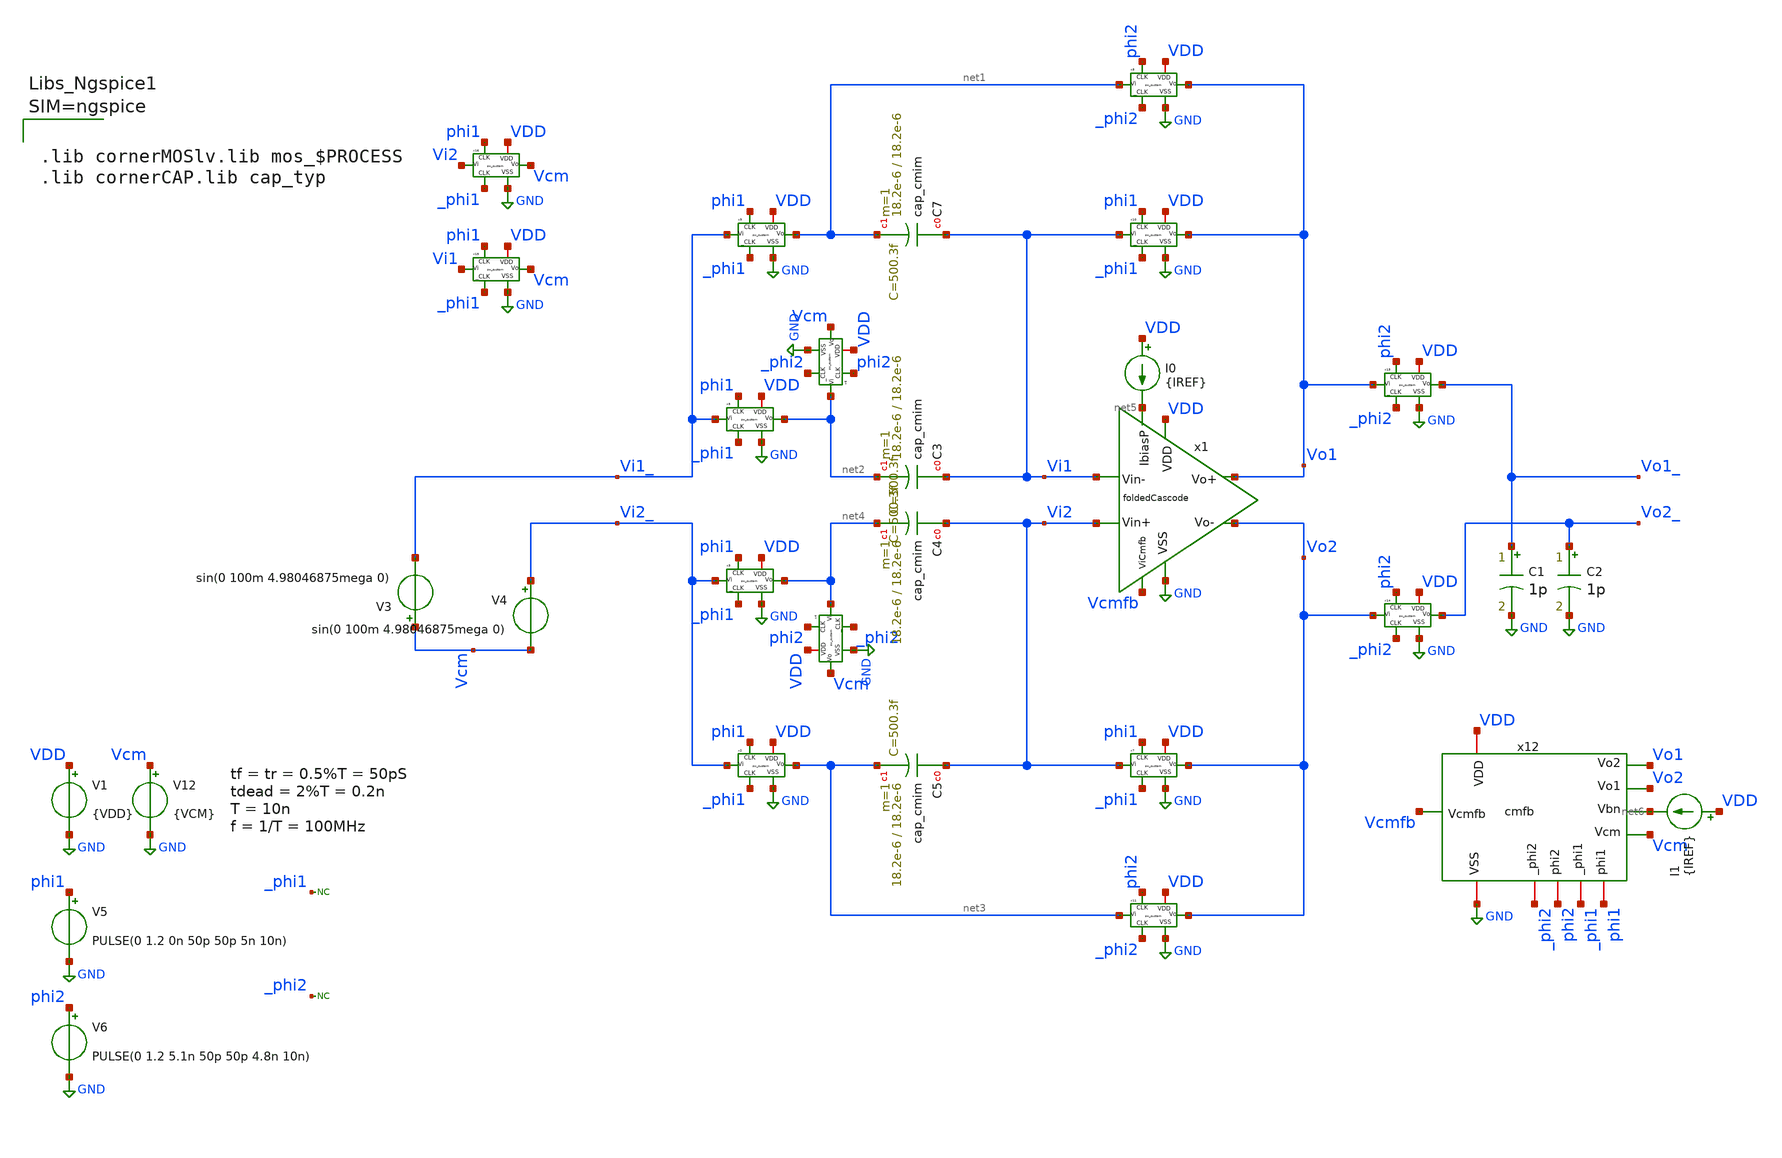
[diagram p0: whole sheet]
** sch_path: sch/AutoTestbench/tb/closeLoop.sch
**.subckt closeLoop
x1 VDD GND Vcmfb net5 Vo1 Vo2 Vi1 Vi2 foldedCascode
V1 VDD GND {VDD}
I0 VDD net5 {IREF}
V5 phi1 GND PULSE(0 1.2 0n 50p 50p 5n 10n)
V6 phi2 GND PULSE(0 1.2 5.1n 50p 50p 4.8n 10n)
x2 phi1 GND net3 Vi2_ VDD _phi1 sw_custom
x3 phi1 GND net4 Vi2_ VDD _phi1 sw_custom
x6 phi2 GND Vcm net2 VDD _phi2 sw_custom
x7 phi1 GND Vo2 Vi2 VDD _phi1 sw_custom
x8 phi2 GND Vo1 net1 VDD _phi2 sw_custom
x10 phi1 GND Vo1 Vi1 VDD _phi1 sw_custom
x9 phi1 GND net1 Vi1_ VDD _phi1 sw_custom
x11 phi2 GND Vo2 net3 VDD _phi2 sw_custom
x12 VDD GND phi1 _phi1 phi2 _phi2 Vcm net6 Vcmfb Vo2 Vo1 cmfb
x5 phi1 GND net2 Vi1_ VDD _phi1 sw_custom
x13 phi2 GND Vo1_ Vo1 VDD _phi2 sw_custom
x14 phi2 GND Vo2_ Vo2 VDD _phi2 sw_custom
V12 Vcm GND {VCM}
x15 phi1 GND Vcm Vi1 VDD _phi1 sw_custom
x16 phi1 GND Vcm Vi2 VDD _phi1 sw_custom
V3 Vcm Vi1_ sin(0 100m 4.98046875mega 0)
V4 Vi2_ Vcm sin(0 100m 4.98046875mega 0)
C1 Vo1_ GND 1p m=1
C2 Vo2_ GND 1p m=1
x4 phi2 GND Vcm net4 VDD _phi2 sw_custom
* noconn _phi1
* noconn _phi2
XC7 Vi1 net1 cap_cmim w=18.2e-6 l=18.2e-6 m=1 mm_ok=1
XC3 Vi1 net2 cap_cmim w=18.2e-6 l=18.2e-6 m=1 mm_ok=1
XC4 Vi2 net4 cap_cmim w=18.2e-6 l=18.2e-6 m=1 mm_ok=1
XC5 Vi2 net3 cap_cmim w=18.2e-6 l=18.2e-6 m=1 mm_ok=1
I1 VDD net6 {IREF}
**** begin user architecture code



.lib cornerMOSlv.lib mos_$PROCESS
.lib cornerCAP.lib cap_typ





.temp $TEMP
.model SW1 SW(Ron=50 Roff=10G Vt=0.4 Vh=0.1)
.nodeset v(Vo1)=0.6 v(Vo2)=0.6 v(Vi1)=0.6 v(Vi2)=0.6
.param VDD=$VDD
.param IREF=$IREF
.param VCM=$VCM
.control
op
tran 100p 12u
let vcm = (v(Vo1) + v(Vo2)) / 2
meas tran vcm_avg AVG vcm FROM=1u TO=3u
let Vinn = v(Vi1_)-v(Vi2_)
let Voutt = v(Vo1_)-v(Vo2_)
meas tran vin_pp  PP Vinn from=1u to=3u
meas tran vout_pp PP Voutt from=1u to=3u

let gain = vout_pp/vin_pp
print gain

let vcm_ = vcm_avg

echo Gain $&gain > results.txt
echo Vcm $&vcm_ >> results.txt

plot v(Vo1_)-v(Vo2_) v(phi2)

plot gain

write closeLoop.raw
*plot v(Vo1_) v(phi1)
plot v(Vo1_) v(Vi1_)
plot V(Vcmfb)
*plot v(Vo1)
plot v(vo1)
plot v(Vo1_)-v(Vo2_)
plot v(Vo1_) v(phi1) v(phi2)
*plot phi1 phi2


wrdata output.txt v(phi1) v(phi2) v(Vi1_) v(Vi2_) v(Vo1_) v(Vo2_)

.endc


**** end user architecture code
**.ends

* expanding   symbol:  foldedCascode.sym # of pins=8
** sym_path: sch/blocks/foldedCascode.sym
** sch_path: sch/blocks/foldedCascode.sch
.subckt foldedCascode VDD VSS ViCmfb IbiasP Vo+ Vo- Vin- Vin+
*.iopin VSS
*.iopin VDD
*.ipin ViCmfb
*.iopin IbiasP
*.ipin Vin+
*.ipin Vin-
*.iopin Vo+
*.iopin Vo-
x1 VDD Vb1_1 Vb1_2 Vx Vy VSS IbiasN gmBoosting
XM1 Vy Vin+ net3 net3 sg13_lv_pmos w=115u l=0.13u ng=100 m=2 mm_ok=1
XM2 Vx Vin- net3 net3 sg13_lv_pmos w=115u l=0.13u ng=100 m=2 mm_ok=1
XM3 Vo+ Vb1_1 Vx VSS sg13_lv_nmos w=44.4u l=0.3u ng=22 m=6 mm_ok=1
XM12 Vx ViCmfb VSS VSS sg13_lv_nmos w=24.3u l=0.8u ng=62 m=6 mm_ok=1
XM4 Vo- Vb1_2 Vy VSS sg13_lv_nmos w=44.4u l=0.3u ng=22 m=6 mm_ok=1
XM5 Vy ViCmfb VSS VSS sg13_lv_nmos w=24.3u l=0.8u ng=62 m=6 mm_ok=1
XM6 Vb0 Vb0 net4 VDD sg13_lv_pmos w=65u l=0.13u ng=65 m=1 mm_ok=1
XM13 net4 Vb0 VDD VDD sg13_lv_pmos w=26u l=0.3u ng=5 m=1 mm_ok=1
XM20 Vb3 Vb2 net6 VDD sg13_lv_pmos w=5.6u l=0.4u ng=1 m=1 mm_ok=1
XM21 net6 Vb3 VDD VDD sg13_lv_pmos w=9.7u l=0.8u ng=2 m=1 mm_ok=1
XM14 IbiasP IbiasP VSS VSS sg13_lv_nmos w=2u l=1u ng=2 m=10 mm_ok=1
XM11 Vb0 IbiasP VSS VSS sg13_lv_nmos w=2u l=1u ng=2 m=2 mm_ok=1
XM15 Vb3 IbiasP VSS VSS sg13_lv_nmos w=2u l=1u ng=2 m=2 mm_ok=1
XM16 Vb2 IbiasP VSS VSS sg13_lv_nmos w=2u l=1u ng=2 m=5 mm_ok=1
XM22 IbiasN IbiasP VSS VSS sg13_lv_nmos w=1.8u l=1u ng=2 m=10 mm_ok=1
XM23 net1 Vb3 VDD VDD sg13_lv_pmos w=63.2u l=0.8u ng=103 m=4 mm_ok=1
XM9 net2 Vb3 VDD VDD sg13_lv_pmos w=63.2u l=0.8u ng=103 m=4 mm_ok=1
XM10 Vo+ Vb2 net1 VDD sg13_lv_pmos w=100u l=0.4u ng=150 m=4 mm_ok=1
XM7 Vo- Vb2 net2 VDD sg13_lv_pmos w=100u l=0.4u ng=150 m=4 mm_ok=1
XM8 net5 Vb2 VDD VDD sg13_lv_pmos w=5.8u l=0.7u ng=1 m=1 mm_ok=1
XM17 Vb2 Vb2 net5 VDD sg13_lv_pmos w=27u l=0.4u ng=9 m=1 mm_ok=1
XM0 net3 Vb0 VDD VDD sg13_lv_pmos w=113.5u l=0.3u ng=210 m=8 mm_ok=1
.ends


* expanding   symbol:  sw_custom.sym # of pins=6
** sym_path: sch/blocks/sw_custom.sym
** sch_path: sch/blocks/sw_custom.sch
.subckt sw_custom CLK VSS Vo Vi VDD _CLK
*.iopin VSS
*.ipin CLK
*.ipin _CLK
*.iopin Vi
*.iopin Vo
*.iopin VDD
S1 Vi Vo CLK VSS SW1
.ends


* expanding   symbol:  cmfb.sym # of pins=11
** sym_path: sch/blocks/cmfb.sym
** sch_path: sch/blocks/cmfb.sch
.subckt cmfb VDD VSS phi1 _phi1 phi2 _phi2 Vcm Vbn Vcmfb Vo1 Vo2
*.iopin VDD
*.iopin VSS
*.iopin phi1
*.iopin _phi1
*.iopin phi2
*.iopin _phi2
*.ipin Vcm
*.ipin Vbn
*.opin Vcmfb
*.ipin Vo1
*.ipin Vo2
x15 phi1 VSS Vcmfb Vbn VDD _phi1 sw_custom
C6 net1 Vcmfb 100f m=1
x16 phi1 VSS net1 Vcm VDD _phi1 sw_custom
C7 net2 Vcmfb 100f m=1
x1 phi1 VSS net2 Vcm VDD _phi1 sw_custom
x2 phi2 VSS net2 Vo1 VDD _phi2 sw_custom
x3 phi2 VSS net1 Vo2 VDD _phi2 sw_custom
.ends


* expanding   symbol:  gmBoosting.sym # of pins=7
** sym_path: sch/blocks/gmBoosting.sym
** sch_path: sch/blocks/gmBoosting.sch
.subckt gmBoosting VDD Vo2 Vo1 Vi+ Vi- VSS IbiasN
*.iopin VSS
*.opin Vo1
*.opin Vo2
*.ipin Vi+
*.ipin Vi-
*.iopin VDD
*.ipin IbiasN
XM7 net2 Vb4 VDD VDD sg13_lv_pmos w=19.8u l=0.7u ng=20 m=2 mm_ok=1
XM1 net7 Vi+ net1 net1 sg13_lv_pmos w=35u l=0.15u ng=70 m=4 mm_ok=1
XM2 net4 Vi- net1 net1 sg13_lv_pmos w=35u l=0.15u ng=70 m=4 mm_ok=1
XM0 net1 Vb0 net5 VDD sg13_lv_pmos w=12u l=0.3u ng=12 m=1 mm_ok=1
XM6 net7 Vb3 VSS VSS sg13_lv_nmos w=20.2u l=0.7u ng=5 m=2 mm_ok=1
XM9 Vo1 Vb2 net2 VDD sg13_lv_pmos w=23.2u l=0.3u ng=10 m=1 mm_ok=1
XM10 Vo2 Vb2 net3 VDD sg13_lv_pmos w=23.2u l=0.3u ng=10 m=1 mm_ok=1
XM3 net5 Vo2 VDD VDD sg13_lv_pmos w=20u l=0.13u ng=5 m=1 mm_ok=1
XM4 net5 Vo1 VDD VDD sg13_lv_pmos w=20u l=0.13u ng=5 m=1 mm_ok=1
XM5 net6 Va VDD VDD sg13_lv_pmos w=20u l=0.13u ng=5 m=2 mm_ok=1
XM29 Vb3 Vb3 VSS VSS sg13_lv_nmos w=32u l=0.7u ng=4 m=1 mm_ok=1
XM30 Vb3 Vb0 net6 VDD sg13_lv_pmos w=12u l=0.3u ng=12 m=1 mm_ok=1
XM31 net4 Vb3 VSS VSS sg13_lv_nmos w=20.2u l=0.7u ng=5 m=2 mm_ok=1
XM32 Vo1 Vb1 net4 VSS sg13_lv_nmos w=38.7u l=0.6u ng=5 m=1 mm_ok=1
XM21 IbiasN IbiasN VDD VDD sg13_lv_pmos w=18u l=1u ng=18 m=1 mm_ok=1
XM24 VbbN IbiasN VDD VDD sg13_lv_pmos w=18u l=1u ng=18 m=1 mm_ok=1
XM25 VbbN VbbN VSS VSS sg13_lv_nmos w=15u l=1u ng=2 m=1 mm_ok=1
XM17 Va VbbN VSS VSS sg13_lv_nmos w=15u l=1u ng=2 m=1 mm_ok=1
XM18 Va Va VDD VDD sg13_lv_pmos w=13u l=1u ng=13 m=1 mm_ok=1
XM19 Vb1 Vb1 net9 VSS sg13_lv_nmos w=13u l=0.7u ng=2 m=1 mm_ok=1
XM20 net9 Vb1 VSS VSS sg13_lv_nmos w=2.4u l=0.7u ng=1 m=1 mm_ok=1
XM22 Vb1 IbiasN VDD VDD sg13_lv_pmos w=18u l=1u ng=18 m=1 mm_ok=1
XM26 Vb4 Vb2 net8 VDD sg13_lv_pmos w=9u l=0.3u ng=9 m=1 mm_ok=1
XM38 net8 Vb4 VDD VDD sg13_lv_pmos w=15.5u l=0.7u ng=15 m=1 mm_ok=1
XM39 Vb4 VbbN VSS VSS sg13_lv_nmos w=15u l=1u ng=2 m=1 mm_ok=1
XM40 net11 Vb2 VDD VDD sg13_lv_pmos w=4.5u l=0.7u ng=1 m=1 mm_ok=1
XM41 Vb2 Vb2 net11 VDD sg13_lv_pmos w=15u l=0.7u ng=15 m=1 mm_ok=1
XM42 Vb2 VbbN VSS VSS sg13_lv_nmos w=15u l=1u ng=2 m=1 mm_ok=1
XM8 net3 Vb4 VDD VDD sg13_lv_pmos w=19.8u l=0.7u ng=20 m=2 mm_ok=1
XM11 Vo2 Vb1 net7 VSS sg13_lv_nmos w=38.7u l=0.6u ng=5 m=1 mm_ok=1
XM12 Vb0 VbbN VSS VSS sg13_lv_nmos w=15u l=1u ng=2 m=1 mm_ok=1
XM13 net10 Vb0 VDD VDD sg13_lv_pmos w=3.92u l=0.7u ng=2 m=1 mm_ok=1
XM14 Vb0 Vb0 net10 VDD sg13_lv_pmos w=55u l=0.15u ng=55 m=1 mm_ok=1
.ends

.GLOBAL GND
**** begin user architecture code
.MODEL SW1 SW   VT=0.9 VH=0.01  RON=0.01 ROFF=10G
**** end user architecture code
.end
